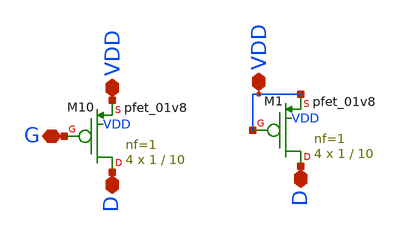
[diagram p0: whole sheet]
** sch_path: magic/second_stage.sch
**.subckt second_stage VDD G D D VDD
*.iopin VDD
*.iopin G
*.iopin D
*.iopin D
*.iopin VDD
XM10 D G VDD VDD sky130_fd_pr__pfet_01v8 L=10 W=1 nf=1 ad='int((nf+1)/2) * W/nf * 0.29' as='int((nf+2)/2) * W/nf * 0.29'
+ pd='2*int((nf+1)/2) * (W/nf + 0.29)' ps='2*int((nf+2)/2) * (W/nf + 0.29)' nrd='0.29 / W' nrs='0.29 / W'
+ sa=0 sb=0 sd=0 mult=4 m=4
XM1 D VDD VDD VDD sky130_fd_pr__pfet_01v8 L=10 W=1 nf=1 ad='int((nf+1)/2) * W/nf * 0.29' as='int((nf+2)/2) * W/nf * 0.29'
+ pd='2*int((nf+1)/2) * (W/nf + 0.29)' ps='2*int((nf+2)/2) * (W/nf + 0.29)' nrd='0.29 / W' nrs='0.29 / W'
+ sa=0 sb=0 sd=0 mult=4 m=4
**.ends
.end
